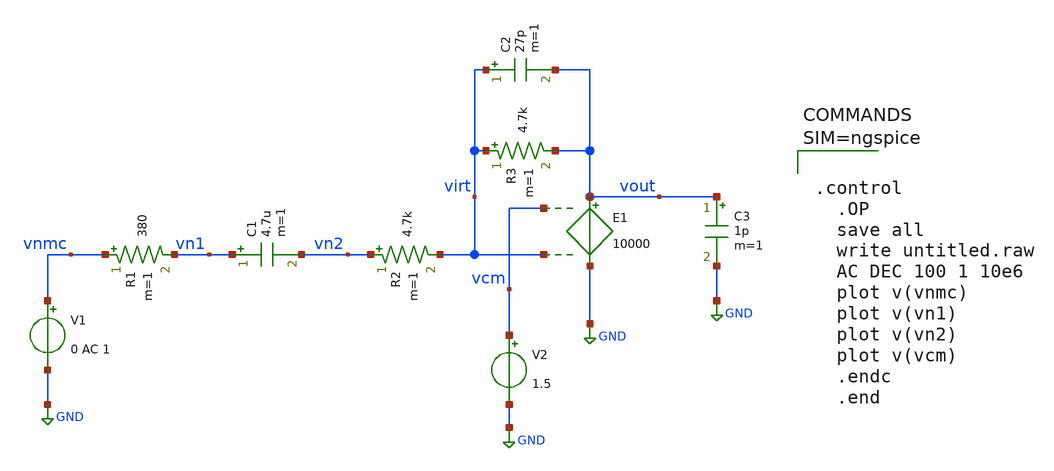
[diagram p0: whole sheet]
** sch_path: xschem/mictest_new.sch
**.subckt mictest_new
V1 vnmc GND 0 AC 1
C1 vn1 vn2 4.7u m=1
R1 vnmc vn1 380 m=1
R2 vn2 virt 4.7k m=1
E1 vout GND vcm virt 10000
R3 virt vout 4.7k m=1
C2 virt vout 27p m=1
V2 vcm GND 1.5
C3 vout GND 1p m=1
**** begin user architecture code



.control
  .OP
  save all
  write untitled.raw
  AC DEC 100 1 10e6
  plot v(vnmc)
  plot v(vn1)
  plot v(vn2)
  plot v(vcm)
  .endc
  .end




**** end user architecture code
**.ends
.GLOBAL GND
.end
